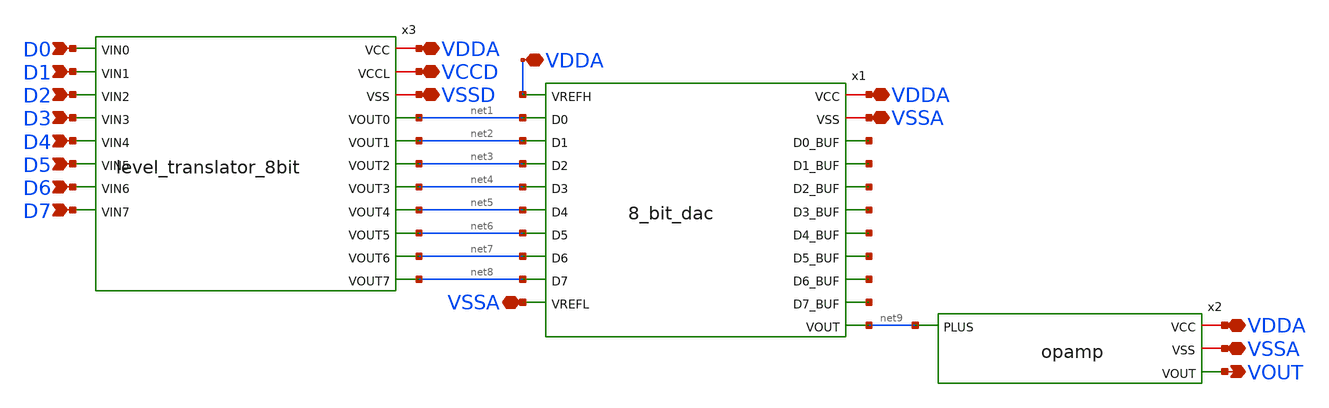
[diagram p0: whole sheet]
** sch_path: All_schematic/dac_top.sch
**.subckt dac_top VDDA VSSD VCCD VDDA VDDA VSSA VSSA VDDA VSSA VOUT D0 D1 D2 D3 D4 D5 D6 D7
*.iopin VDDA
*.iopin VSSD
*.iopin VCCD
*.iopin VDDA
*.iopin VDDA
*.iopin VSSA
*.iopin VSSA
*.iopin VDDA
*.iopin VSSA
*.opin VOUT
*.ipin D0
*.ipin D1
*.ipin D2
*.ipin D3
*.ipin D4
*.ipin D5
*.ipin D6
*.ipin D7
x1 VDDA VDDA VSSA net10 net11 net12 net13 net14 net15 net16 net8 net17 net9 net1 net2 net3 net4 net5
+ net6 net7 VSSA 8_bit_dac
x2 VDDA VSSA net9 VOUT opamp
x3 VDDA VCCD VSSD D0 net1 D1 net2 D2 net3 D3 net4 D4 net5 D5 net6 D6 net7 D7 net8
+ level_translator_8bit
**.ends
.end
